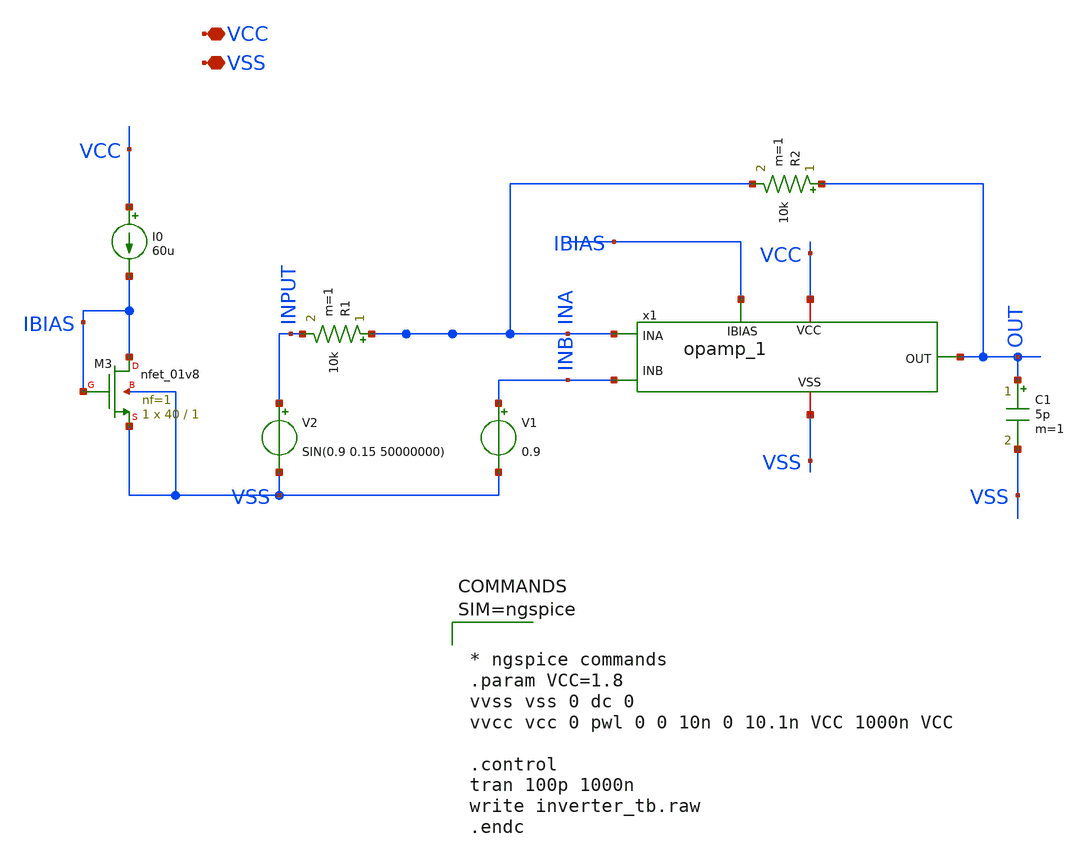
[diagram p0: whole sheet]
** sch_path: xschem/opamp_1_tb.sch
**.subckt opamp_1_tb VCC VSS
*.iopin VCC
*.iopin VSS
x1 VCC OUT INA INB VSS IBIAS opamp_1
V1 INB VSS 0.9
V2 INPUT VSS SIN(0.9 0.15 50000000)
R1 INA INPUT 10k m=1
R2 OUT INA 10k m=1
C1 OUT VSS 5p m=1
XM3 IBIAS IBIAS VSS VSS sky130_fd_pr__nfet_01v8 L=1 W=40 nf=1 ad='int((nf+1)/2) * W/nf * 0.29' as='int((nf+2)/2) * W/nf * 0.29'
+ pd='2*int((nf+1)/2) * (W/nf + 0.29)' ps='2*int((nf+2)/2) * (W/nf + 0.29)' nrd='0.29 / W' nrs='0.29 / W'
+ sa=0 sb=0 sd=0 mult=1 m=1
I0 VCC IBIAS 60u
**** begin user architecture code

** opencircuitdesign pdks install
.lib $::SKYWATER_MODELS/sky130.lib.spice tt





* ngspice commands
.param VCC=1.8
vvss vss 0 dc 0
vvcc vcc 0 pwl 0 0 10n 0 10.1n VCC 1000n VCC

.control
tran 100p 1000n
write inverter_tb.raw
.endc




**** end user architecture code
**.ends

* expanding   symbol:  opamp_1.sym # of pins=6
** sym_path: xschem/opamp_1.sym
** sch_path: xschem/opamp_1.sch
.subckt opamp_1 VCC OUT INA INB VSS IBIAS
*.ipin INA
*.ipin INB
*.opin OUT
*.iopin VCC
*.iopin VSS
*.ipin IBIAS
XM1 MIRR INA TAILV VSS sky130_fd_pr__nfet_01v8 L=1 W=20 nf=1 ad='int((nf+1)/2) * W/nf * 0.29' as='int((nf+2)/2) * W/nf * 0.29'
+ pd='2*int((nf+1)/2) * (W/nf + 0.29)' ps='2*int((nf+2)/2) * (W/nf + 0.29)' nrd='0.29 / W' nrs='0.29 / W'
+ sa=0 sb=0 sd=0 mult=1 m=1
XM2 DIFF_OUT INB TAILV VSS sky130_fd_pr__nfet_01v8 L=1 W=20 nf=1 ad='int((nf+1)/2) * W/nf * 0.29' as='int((nf+2)/2) * W/nf * 0.29'
+ pd='2*int((nf+1)/2) * (W/nf + 0.29)' ps='2*int((nf+2)/2) * (W/nf + 0.29)' nrd='0.29 / W' nrs='0.29 / W'
+ sa=0 sb=0 sd=0 mult=1 m=1
XM3 TAILV IBIAS VSS VSS sky130_fd_pr__nfet_01v8 L=1 W=40 nf=1 ad='int((nf+1)/2) * W/nf * 0.29' as='int((nf+2)/2) * W/nf * 0.29'
+ pd='2*int((nf+1)/2) * (W/nf + 0.29)' ps='2*int((nf+2)/2) * (W/nf + 0.29)' nrd='0.29 / W' nrs='0.29 / W'
+ sa=0 sb=0 sd=0 mult=1 m=1
XM4 MIRR MIRR VCC VCC sky130_fd_pr__pfet_01v8_lvt L=0.5 W=14 nf=1 ad='int((nf+1)/2) * W/nf * 0.29' as='int((nf+2)/2) * W/nf * 0.29'
+ pd='2*int((nf+1)/2) * (W/nf + 0.29)' ps='2*int((nf+2)/2) * (W/nf + 0.29)' nrd='0.29 / W' nrs='0.29 / W'
+ sa=0 sb=0 sd=0 mult=1 m=1
XM5 DIFF_OUT MIRR VCC VCC sky130_fd_pr__pfet_01v8_lvt L=0.5 W=14 nf=1 ad='int((nf+1)/2) * W/nf * 0.29'
+ as='int((nf+2)/2) * W/nf * 0.29' pd='2*int((nf+1)/2) * (W/nf + 0.29)' ps='2*int((nf+2)/2) * (W/nf + 0.29)'
+ nrd='0.29 / W' nrs='0.29 / W' sa=0 sb=0 sd=0 mult=1 m=1
XM6 OUT IBIAS VSS VSS sky130_fd_pr__nfet_01v8 L=0.5 W=93 nf=1 ad='int((nf+1)/2) * W/nf * 0.29' as='int((nf+2)/2) * W/nf * 0.29'
+ pd='2*int((nf+1)/2) * (W/nf + 0.29)' ps='2*int((nf+2)/2) * (W/nf + 0.29)' nrd='0.29 / W' nrs='0.29 / W'
+ sa=0 sb=0 sd=0 mult=1 m=1
XM7 OUT DIFF_OUT VCC VCC sky130_fd_pr__pfet_01v8_lvt L=0.5 W=70 nf=1 ad='int((nf+1)/2) * W/nf * 0.29'
+ as='int((nf+2)/2) * W/nf * 0.29' pd='2*int((nf+1)/2) * (W/nf + 0.29)' ps='2*int((nf+2)/2) * (W/nf + 0.29)'
+ nrd='0.29 / W' nrs='0.29 / W' sa=0 sb=0 sd=0 mult=1 m=1
XM9 RBIAS IBIAS VSS VSS sky130_fd_pr__nfet_01v8 L=1 W=5 nf=1 ad='int((nf+1)/2) * W/nf * 0.29' as='int((nf+2)/2) * W/nf * 0.29'
+ pd='2*int((nf+1)/2) * (W/nf + 0.29)' ps='2*int((nf+2)/2) * (W/nf + 0.29)' nrd='0.29 / W' nrs='0.29 / W'
+ sa=0 sb=0 sd=0 mult=1 m=1
XM10 RBIAS RBIAS net2 VCC sky130_fd_pr__pfet_01v8_lvt L=0.5 W=1 nf=1 ad='int((nf+1)/2) * W/nf * 0.29'
+ as='int((nf+2)/2) * W/nf * 0.29' pd='2*int((nf+1)/2) * (W/nf + 0.29)' ps='2*int((nf+2)/2) * (W/nf + 0.29)'
+ nrd='0.29 / W' nrs='0.29 / W' sa=0 sb=0 sd=0 mult=1 m=1
XM11 net2 net2 VCC VCC sky130_fd_pr__pfet_01v8_lvt L=0.5 W=7.5 nf=1 ad='int((nf+1)/2) * W/nf * 0.29'
+ as='int((nf+2)/2) * W/nf * 0.29' pd='2*int((nf+1)/2) * (W/nf + 0.29)' ps='2*int((nf+2)/2) * (W/nf + 0.29)'
+ nrd='0.29 / W' nrs='0.29 / W' sa=0 sb=0 sd=0 mult=1 m=1
XC1 OUT net1 sky130_fd_pr__cap_mim_m3_2 W=20 L=13 MF=1 m=1
XM8 net1 RBIAS DIFF_OUT VCC sky130_fd_pr__pfet_01v8_lvt L=0.5 W=14 nf=1 ad='int((nf+1)/2) * W/nf * 0.29'
+ as='int((nf+2)/2) * W/nf * 0.29' pd='2*int((nf+1)/2) * (W/nf + 0.29)' ps='2*int((nf+2)/2) * (W/nf + 0.29)'
+ nrd='0.29 / W' nrs='0.29 / W' sa=0 sb=0 sd=0 mult=1 m=1
.ends

.end
